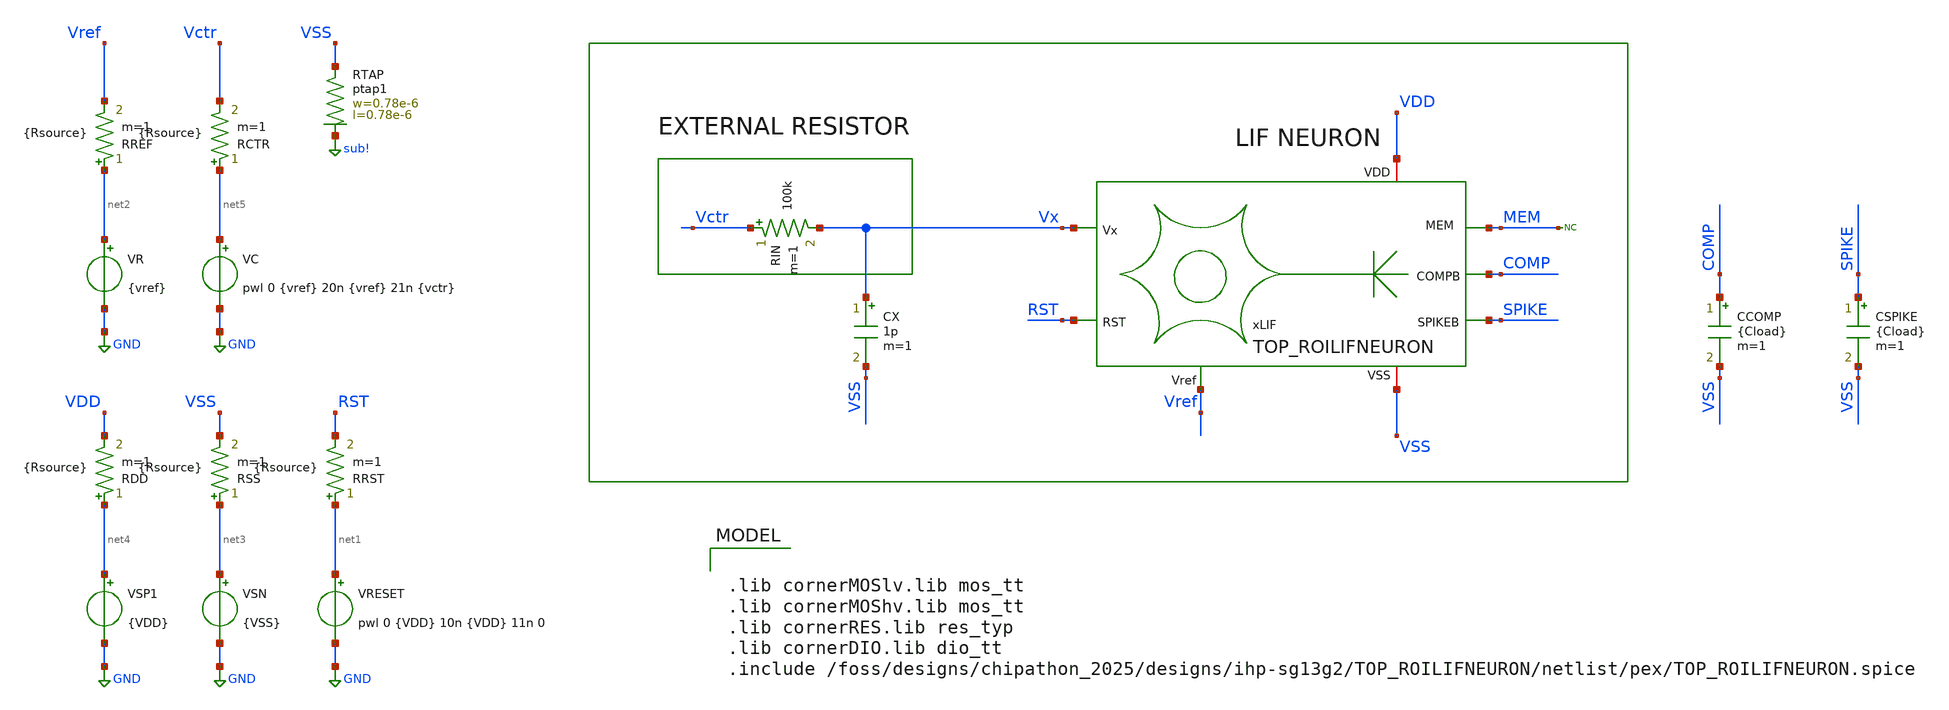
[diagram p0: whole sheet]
** sch_path: work/TOP_ROILIFNEURON/xschem/TOP_ROILIFNEURON_TB.sch
**.subckt TOP_ROILIFNEURON_TB
VRESET net1 GND pwl 0 {VDD} 10n {VDD} 11n 0
VSN net3 GND {VSS}
VR net2 GND {vref}
VC net5 GND pwl 0 {vref} 20n {vref} 21n {vctr}
RDD net4 VDD {Rsource} m=1
RSS net3 VSS {Rsource} m=1
RRST net1 RST {Rsource} m=1
RREF net2 Vref {Rsource} m=1
RCTR net5 Vctr {Rsource} m=1
CSPIKE SPIKE VSS {Cload} m=1
RIN Vctr Vx 100k m=1
VSP1 net4 GND {VDD}
* noconn MEM
XRTAP VSS sub! ptap1 R=262.8 w=0.78e-6 l=0.78e-6
CX Vx VSS 1p m=1
CCOMP COMP VSS {Cload} m=1
xLIF VDD Vx MEM RST SPIKE VSS Vref COMP TOP_ROILIFNEURON
**** begin user architecture code



.temp 27
.param VDD = 0.6
.param VSS = 0
.param vctr = 0
.param vref = 0.6
.param Cload = 20p
.param Rsource = 1m

.param sw_stat_global = 0
.param sw_stat_mismatch = 0

*.save @v.xLIF.VINT[i]
*.save @v.xLIF.VCOMP[i]
*.save @v.xLIF.VSPIKE[i]

.save all

.control

* >> Variables <<
let Vhigh = 0.5
let Vmid = Vhigh * 0.5
let tstop = 0.1u
let tstep = tstop/10k

* Run transient analysis
tran $&tstep $&tstop uic

* Average current
let IDD = -1*i(VSP1)

meas tran I_avg AVG IDD from=11n to=tstop
let P_avg = abs(I_avg*Vhigh)

meas TRAN T_spk TRIG v(SPIKE) VAL=Vmid rise=2 TARG v(SPIKE) VAL=Vmid rise=3
let F_spk = 1 / T_spk
let E_spk = P_avg/F_spk

*Print Neuron results
print F_spk I_avg P_avg E_spk

*Internal currents
*let i_VINT = @v.xLIF.VINT[i]
*let i_VCOMP = @v.xLIF.VCOMP[i]
*let i_VSPIKE = @v.xLIF.VSPIKE[i]

*meas tran i_VINT AVG i_VINT from=11n to=tstop
*meas tran i_VCOMP AVG i_VCOMP from=11n to=tstop
*meas tran i_VSPIKE AVG i_VSPIKE from=11n to=tstop
*print i_VINT i_VCOMP i_VSPIKE

* Plots
plot v(Vctr) v(Vref) v(RST)
plot v(MEM) v(Vx) v(vctr)
plot v(COMP) v(SPIKE)

.endc



.lib cornerMOSlv.lib mos_tt
.lib cornerMOShv.lib mos_tt
.lib cornerRES.lib res_typ
.lib cornerDIO.lib dio_tt
.include /foss/designs/chipathon_2025/designs/ihp-sg13g2/TOP_ROILIFNEURON/netlist/pex/TOP_ROILIFNEURON.spice

**** end user architecture code
**.ends
.GLOBAL GND
.GLOBAL sub!
.end
